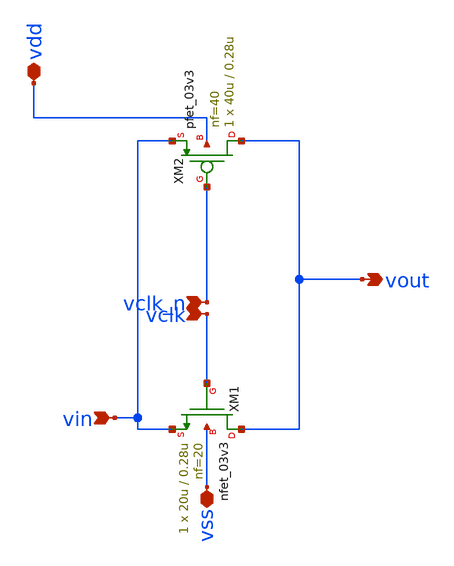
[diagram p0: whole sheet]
** sch_path: analog/blocks/transmission_gate/transmission_gate.sch
**.subckt transmission_gate vclk vin vdd vss vout vclk_n
*.ipin vclk
*.ipin vin
*.iopin vdd
*.iopin vss
*.opin vout
*.ipin vclk_n
XM1 vout vclk vin vss nfet_03v3 L=0.28u W=20u nf=20 ad='int((nf+1)/2) * W/nf * 0.18u' as='int((nf+2)/2) * W/nf * 0.18u'
+ pd='2*int((nf+1)/2) * (W/nf + 0.18u)' ps='2*int((nf+2)/2) * (W/nf + 0.18u)' nrd='0.18u / W' nrs='0.18u / W'
+ sa=0 sb=0 sd=0 m=1
XM2 vout vclk_n vin vdd pfet_03v3 L=0.28u W=40u nf=40 ad='int((nf+1)/2) * W/nf * 0.18u' as='int((nf+2)/2) * W/nf * 0.18u'
+ pd='2*int((nf+1)/2) * (W/nf + 0.18u)' ps='2*int((nf+2)/2) * (W/nf + 0.18u)' nrd='0.18u / W' nrs='0.18u / W'
+ sa=0 sb=0 sd=0 m=1
**.ends
.end
